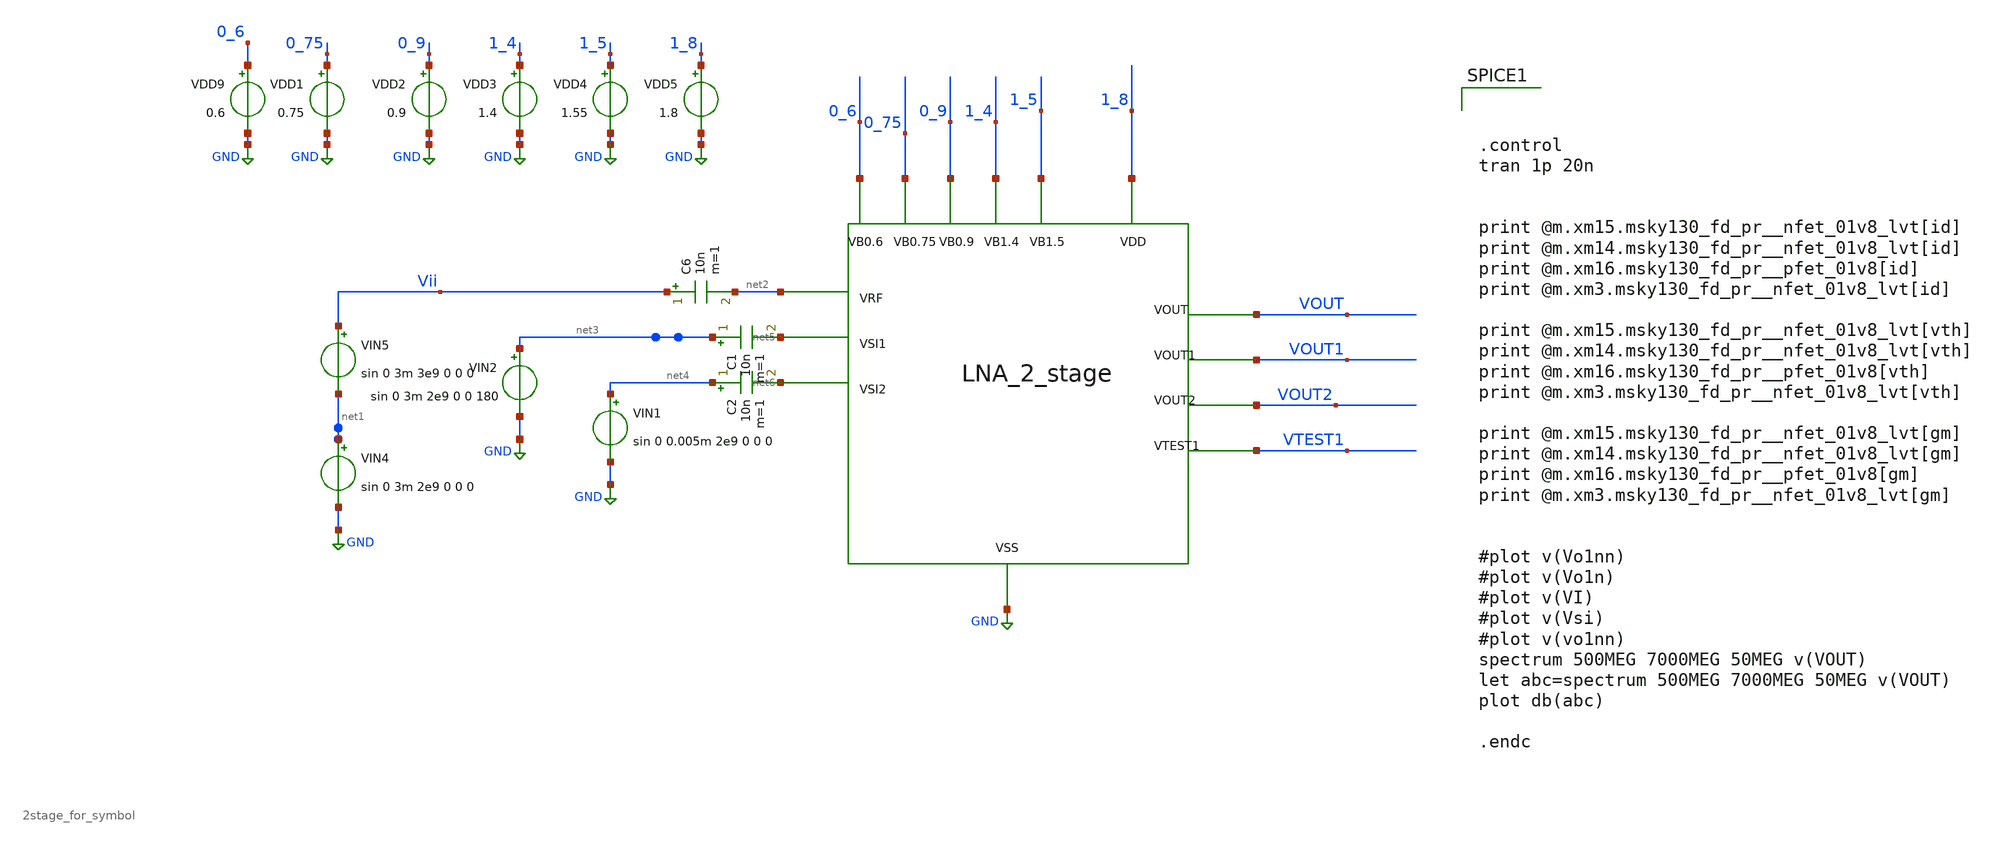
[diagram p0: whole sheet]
** sch_path: xschem/xschem4_sic_final/2stage_tb_sym.sch
**.subckt 2stage_tb_sym
C6 Vii net2 10n m=1
VIN4 net1 GND sin 0 3m 2e9 0 0 0
VIN5 Vii net1 sin 0 3m 3e9 0 0 0
VIN2 net3 GND sin 0 3m 2e9 0 0 180
C1 net3 net5 10n m=1
VIN1 net4 GND sin 0 0.005m 2e9 0 0 0
C2 net4 net6 10n m=1
VDD9 0_6 GND 0.6
VDD1 0_75 GND 0.75
VDD2 0_9 GND 0.9
VDD3 1_4 GND 1.4
VDD4 1_5 GND 1.55
VDD5 1_8 GND 1.8
X1 1_8 GND VOUT VOUT1 VOUT2 VTEST1 net2 net5 net6 0_75 1_5 1_4 0_9 0_6 2stage_for_symbol
**** begin user architecture code



.control
tran 1p 20n


print @m.xm15.msky130_fd_pr__nfet_01v8_lvt[id]
print @m.xm14.msky130_fd_pr__nfet_01v8_lvt[id]
print @m.xm16.msky130_fd_pr__pfet_01v8[id]
print @m.xm3.msky130_fd_pr__nfet_01v8_lvt[id]

print @m.xm15.msky130_fd_pr__nfet_01v8_lvt[vth]
print @m.xm14.msky130_fd_pr__nfet_01v8_lvt[vth]
print @m.xm16.msky130_fd_pr__pfet_01v8[vth]
print @m.xm3.msky130_fd_pr__nfet_01v8_lvt[vth]

print @m.xm15.msky130_fd_pr__nfet_01v8_lvt[gm]
print @m.xm14.msky130_fd_pr__nfet_01v8_lvt[gm]
print @m.xm16.msky130_fd_pr__pfet_01v8[gm]
print @m.xm3.msky130_fd_pr__nfet_01v8_lvt[gm]


#plot v(Vo1nn)
#plot v(Vo1n)
#plot v(VI)
#plot v(Vsi)
#plot v(vo1nn)
spectrum 500MEG 7000MEG 50MEG v(VOUT)
let abc=spectrum 500MEG 7000MEG 50MEG v(VOUT)
plot db(abc)

.endc



.lib $::SKYWATER_MODELS/sky130.lib.spice tt

**** end user architecture code
**.ends

* expanding   symbol:  2stage_for_symbol.sym # of pins=14
** sym_path: xschem/xschem4_sic_final/2stage_for_symbol.sym
** sch_path: xschem/xschem4_sic_final/2stage_for_symbol.sch
.subckt 2stage_for_symbol VDD VSS VOUT VOUT1 VOUT2 VTEST1 VRF VSI1 VSI2 VB0_75 VB1_5 VB1_4 VB0_9
+ VB0_6
*.iopin VRF
*.iopin VSS
*.iopin VB0_75
*.iopin VSI1
*.iopin VDD
*.iopin VOUT1
*.iopin VOUT2
*.iopin VB1_4
*.iopin VB1_5
*.iopin VB0_9
*.iopin VSI2
*.iopin VB0_6
*.iopin VTEST1
*.iopin VOUT
XR4 VB1_5 net1 VSS sky130_fd_pr__res_high_po_0p35 L=4 mult=1 m=1
XC5 net1 VOUT1 sky130_fd_pr__cap_mim_m3_2 W=30 L=30 MF=1 m=1
XM12 VTEST1 VRF VSS VSS sky130_fd_pr__nfet_01v8_lvt L=0.15 W=200 nf=20 ad='int((nf+1)/2) * W/nf * 0.29'
+ as='int((nf+2)/2) * W/nf * 0.29' pd='2*int((nf+1)/2) * (W/nf + 0.29)' ps='2*int((nf+2)/2) * (W/nf + 0.29)'
+ nrd='0.29 / W' nrs='0.29 / W' sa=0 sb=0 sd=0 mult=1 m=1
XM13 VTEST1 VRF VDD VDD sky130_fd_pr__pfet_01v8 L=0.15 W=60 nf=11 ad='int((nf+1)/2) * W/nf * 0.29' as='int((nf+2)/2) * W/nf * 0.29'
+ pd='2*int((nf+1)/2) * (W/nf + 0.29)' ps='2*int((nf+2)/2) * (W/nf + 0.29)' nrd='0.29 / W' nrs='0.29 / W'
+ sa=0 sb=0 sd=0 mult=1 m=1
XM14 VOUT1 VB1_4 VTEST1 VSS sky130_fd_pr__nfet_01v8_lvt L=0.15 W=80 nf=10 ad='int((nf+1)/2) * W/nf * 0.29'
+ as='int((nf+2)/2) * W/nf * 0.29' pd='2*int((nf+1)/2) * (W/nf + 0.29)' ps='2*int((nf+2)/2) * (W/nf + 0.29)'
+ nrd='0.29 / W' nrs='0.29 / W' sa=0 sb=0 sd=0 mult=1 m=1
XM15 net2 net1 VRF VSS sky130_fd_pr__nfet_01v8_lvt L=0.15 W=8 nf=1 ad='int((nf+1)/2) * W/nf * 0.29' as='int((nf+2)/2) * W/nf * 0.29'
+ pd='2*int((nf+1)/2) * (W/nf + 0.29)' ps='2*int((nf+2)/2) * (W/nf + 0.29)' nrd='0.29 / W' nrs='0.29 / W'
+ sa=0 sb=0 sd=0 mult=1 m=1
XM16 VRF VB0_75 VSS VSS sky130_fd_pr__nfet_01v8_lvt L=0.15 W=7.4 nf=1 ad='int((nf+1)/2) * W/nf * 0.29'
+ as='int((nf+2)/2) * W/nf * 0.29' pd='2*int((nf+1)/2) * (W/nf + 0.29)' ps='2*int((nf+2)/2) * (W/nf + 0.29)'
+ nrd='0.29 / W' nrs='0.29 / W' sa=0 sb=0 sd=0 mult=1 m=1
XM17 VOUT net5 VSS VSS sky130_fd_pr__nfet_01v8_lvt L=0.15 W=45 nf=9 ad='int((nf+1)/2) * W/nf * 0.29'
+ as='int((nf+2)/2) * W/nf * 0.29' pd='2*int((nf+1)/2) * (W/nf + 0.29)' ps='2*int((nf+2)/2) * (W/nf + 0.29)'
+ nrd='0.29 / W' nrs='0.29 / W' sa=0 sb=0 sd=0 mult=1 m=1
XM18 VDD net3 VOUT VSS sky130_fd_pr__nfet_01v8_lvt L=0.15 W=4 nf=1 ad='int((nf+1)/2) * W/nf * 0.29' as='int((nf+2)/2) * W/nf * 0.29'
+ pd='2*int((nf+1)/2) * (W/nf + 0.29)' ps='2*int((nf+2)/2) * (W/nf + 0.29)' nrd='0.29 / W' nrs='0.29 / W'
+ sa=0 sb=0 sd=0 mult=3 m=3
XR11 net3 VDD VSS sky130_fd_pr__res_high_po_0p35 L=15 mult=1 m=1
XM19 VOUT net4 VDD VDD sky130_fd_pr__pfet_01v8 L=0.15 W=5 nf=1 ad='int((nf+1)/2) * W/nf * 0.29' as='int((nf+2)/2) * W/nf * 0.29'
+ pd='2*int((nf+1)/2) * (W/nf + 0.29)' ps='2*int((nf+2)/2) * (W/nf + 0.29)' nrd='0.29 / W' nrs='0.29 / W'
+ sa=0 sb=0 sd=0 mult=16 m=16
XC7 VOUT2 net3 sky130_fd_pr__cap_mim_m3_2 W=30 L=30 MF=1 m=1
XR12 VB0_9 net5 VSS sky130_fd_pr__res_high_po_0p35 L=8 mult=1 m=1
XC8 VOUT1 net5 sky130_fd_pr__cap_mim_m3_2 W=30 L=30 MF=1 m=1
XR13 VB0_6 net4 VSS sky130_fd_pr__res_high_po_0p35 L=15 mult=1 m=1
XR14 net2 VDD VSS sky130_fd_pr__res_high_po_0p35 L=0.5 mult=1 m=1
XM20 VTEST1 VSI1 VSS VSS sky130_fd_pr__nfet_01v8_lvt L=0.15 W=220 nf=20 ad='int((nf+1)/2) * W/nf * 0.29'
+ as='int((nf+2)/2) * W/nf * 0.29' pd='2*int((nf+1)/2) * (W/nf + 0.29)' ps='2*int((nf+2)/2) * (W/nf + 0.29)'
+ nrd='0.29 / W' nrs='0.29 / W' sa=0 sb=0 sd=0 mult=1 m=1
XR15 VOUT1 VDD VSS sky130_fd_pr__res_high_po_0p69 L=0.69 mult=8 m=8
XR16 VB0_75 VSI1 VSS sky130_fd_pr__res_high_po_0p35 L=0.5 mult=1 m=1
XM21 VOUT2 VOUT1 VSS VSS sky130_fd_pr__nfet_01v8_lvt L=0.15 W=8 nf=1 ad='int((nf+1)/2) * W/nf * 0.29'
+ as='int((nf+2)/2) * W/nf * 0.29' pd='2*int((nf+1)/2) * (W/nf + 0.29)' ps='2*int((nf+2)/2) * (W/nf + 0.29)'
+ nrd='0.29 / W' nrs='0.29 / W' sa=0 sb=0 sd=0 mult=1 m=1
XR17 VOUT2 VDD VSS sky130_fd_pr__res_high_po_0p35 L=0.5 mult=1 m=1
XM22 VOUT VSI2 VSS VSS sky130_fd_pr__nfet_01v8_lvt L=0.15 W=80 nf=10 ad='int((nf+1)/2) * W/nf * 0.29'
+ as='int((nf+2)/2) * W/nf * 0.29' pd='2*int((nf+1)/2) * (W/nf + 0.29)' ps='2*int((nf+2)/2) * (W/nf + 0.29)'
+ nrd='0.29 / W' nrs='0.29 / W' sa=0 sb=0 sd=0 mult=1 m=1
XR18 VB0_75 VSI2 VSS sky130_fd_pr__res_high_po_0p35 L=0.5 mult=1 m=1
.ends

.GLOBAL GND
.end
